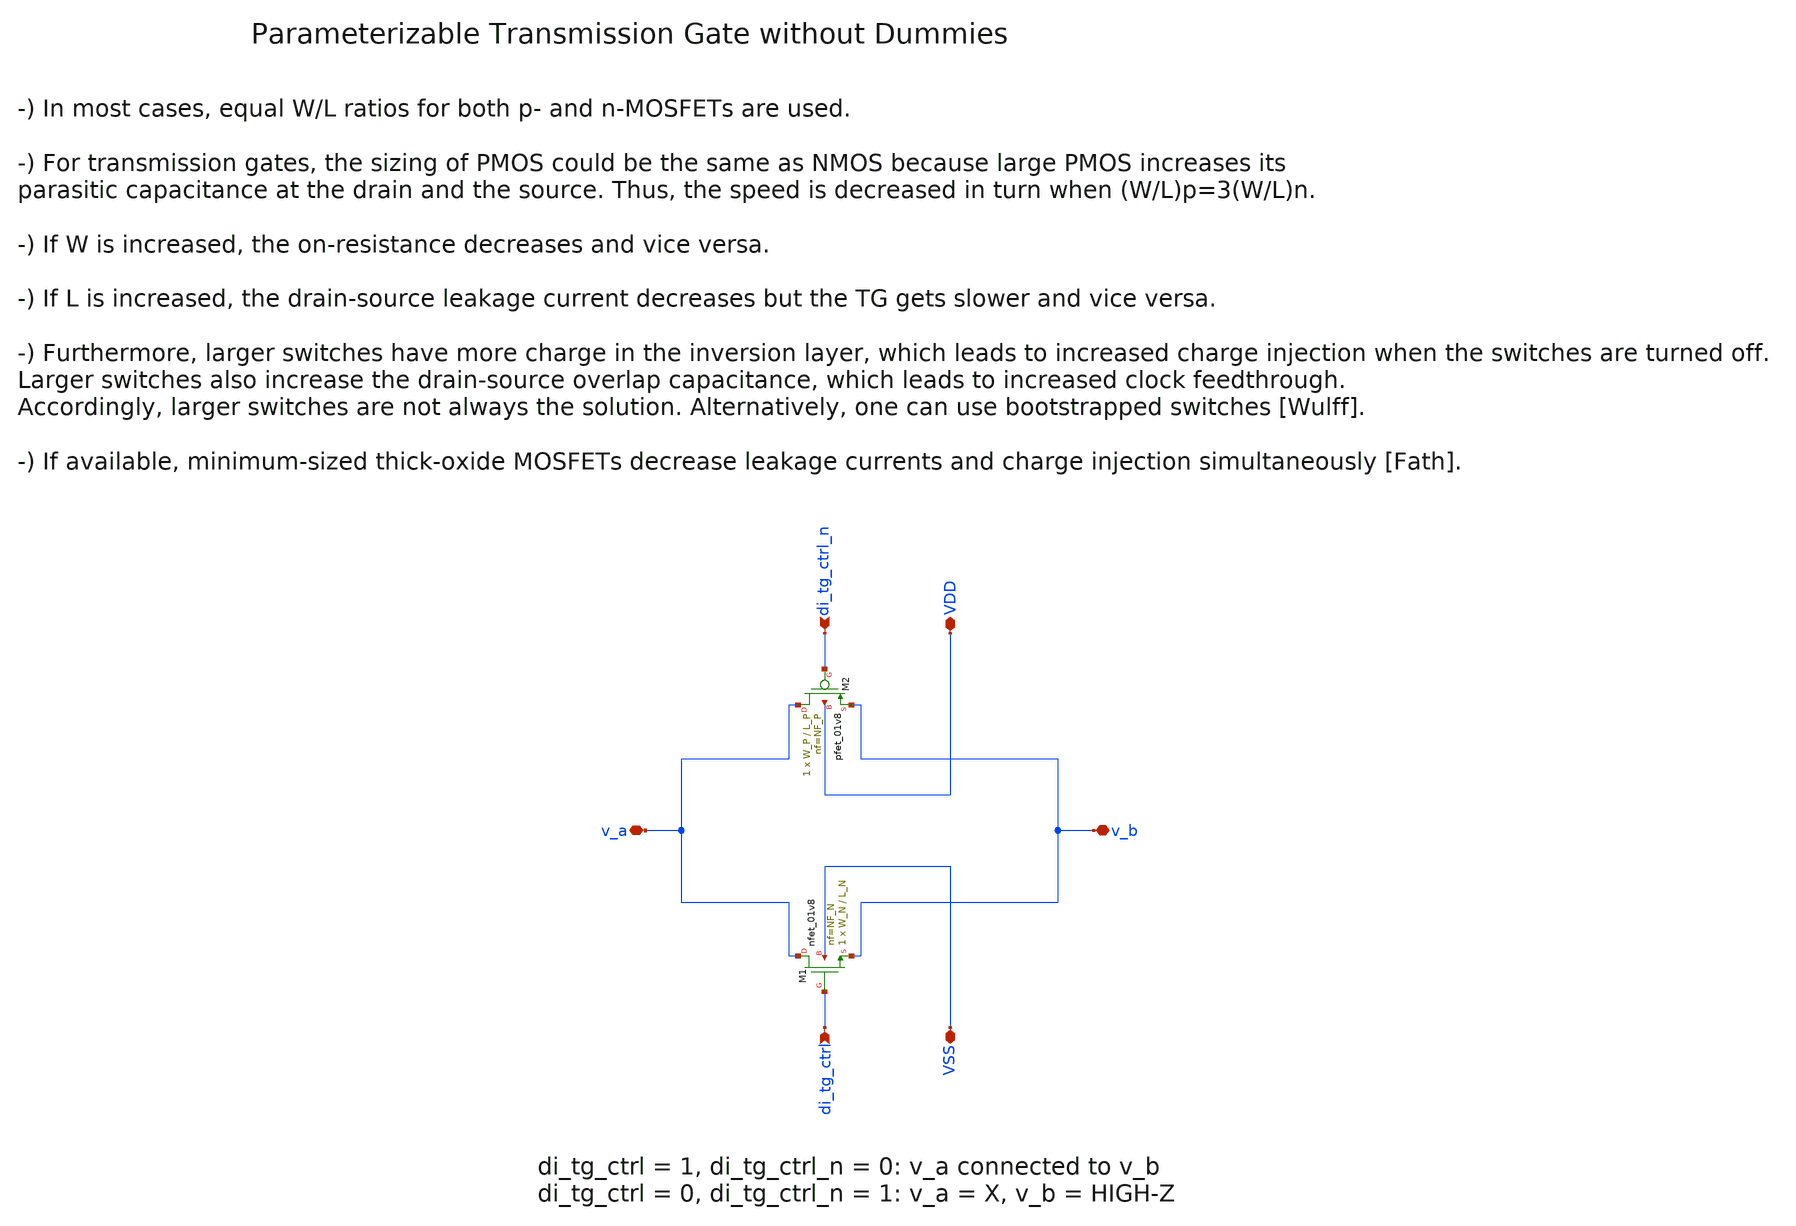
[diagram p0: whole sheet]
** sch_path: sky130/macros/iqmod/schematic/generic/wspr_tx_iqmod_mixer_lo_logic_tg_gen.sch
**.subckt wspr_tx_iqmod_mixer_lo_logic_tg_gen v_a v_b VDD VSS di_tg_ctrl di_tg_ctrl_n
*.iopin v_a
*.iopin v_b
*.iopin VDD
*.iopin VSS
*.ipin di_tg_ctrl
*.ipin di_tg_ctrl_n
XM1 v_a di_tg_ctrl v_b VSS sky130_fd_pr__nfet_01v8 L=L_N W=W_N nf=NF_N ad='int((NF_N + 1)/2) * W_N / NF_N * 0.29'
+ as='int((NF_N + 2)/2) * W_N / NF_N * 0.29' pd='2*int((NF_N + 1)/2) * (W_N / NF_N + 0.29)' ps='2*int((NF_N + 2)/2) * (W_N / NF_N + 0.29)'
+ nrd='0.29 / W_N ' nrs='0.29 / W_N ' sa=0 sb=0 sd=0 mult=1 m=1
XM2 v_a di_tg_ctrl_n v_b VDD sky130_fd_pr__pfet_01v8 L=L_P W=W_P nf=NF_P ad='int((NF_P + 1)/2) * W_P / NF_P * 0.29'
+ as='int((NF_P + 2)/2) * W_P / NF_P * 0.29' pd='2*int((NF_P + 1)/2) * (W_P / NF_P + 0.29)' ps='2*int((NF_P + 2)/2) * (W_P / NF_P + 0.29)'
+ nrd='0.29 / W_P ' nrs='0.29 / W_P ' sa=0 sb=0 sd=0 mult=1 m=1
**.ends
.end
